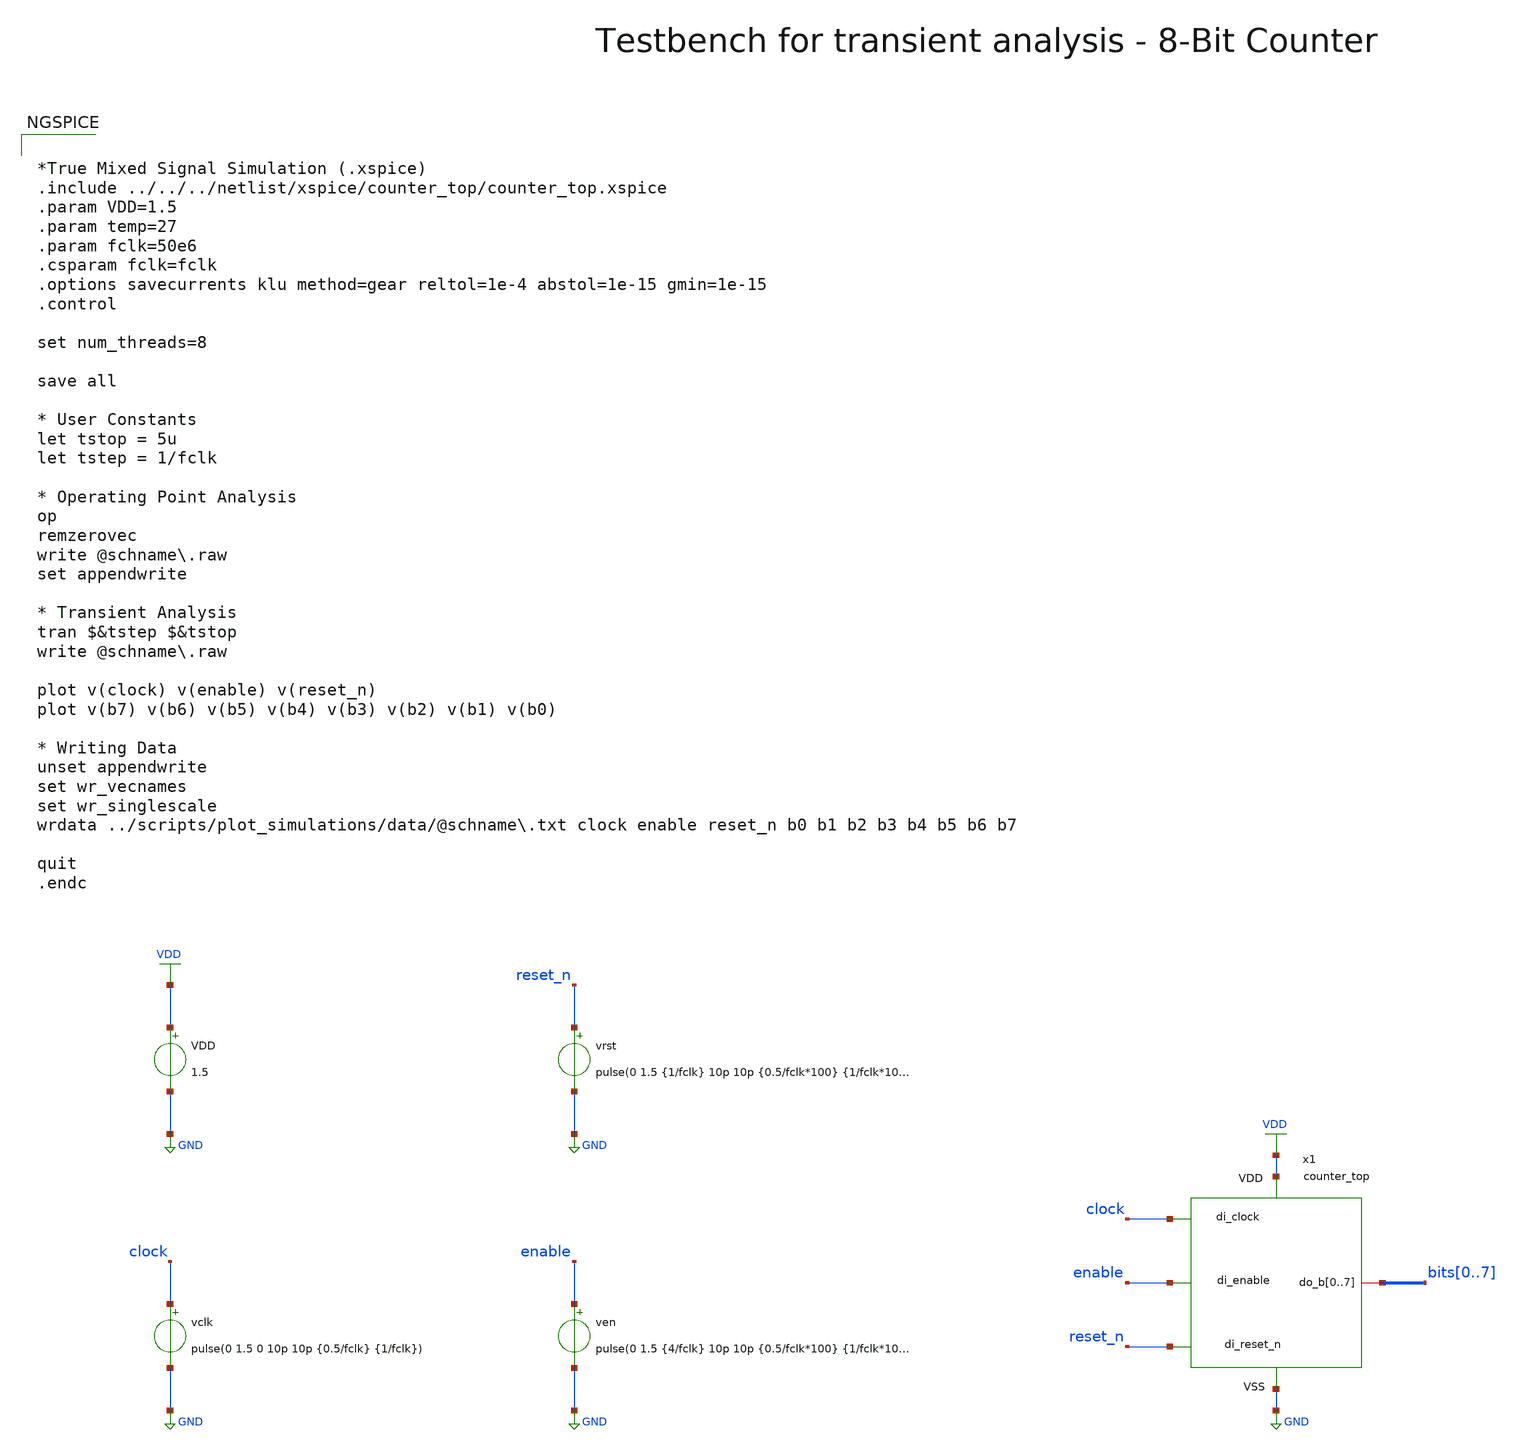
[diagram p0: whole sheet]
** sch_path: macros/counter/testbenches/xschem/counter_top_tb_tran.sch
**.subckt counter_top_tb_tran
VDD VDD GND 1.5
vclk clock GND pulse(0 1.5 0 10p 10p {0.5/fclk} {1/fclk})
vrst reset_n GND pulse(0 1.5 {1/fclk} 10p 10p {0.5/fclk*100} {1/fclk*100})
ven enable GND pulse(0 1.5 {4/fclk} 10p 10p {0.5/fclk*100} {1/fclk*100})
x1 VDD GND clock reset_n enable bits0 bits1 bits2 bits3 bits4 bits5 bits6 bits7 counter_top
**** begin user architecture code


*True Mixed Signal Simulation (.xspice)
.include ../../../netlist/xspice/counter_top/counter_top.xspice
.param VDD=1.5
.param temp=27
.param fclk=50e6
.csparam fclk=fclk
.options savecurrents klu method=gear reltol=1e-4 abstol=1e-15 gmin=1e-15
.control

set num_threads=8

save all

* User Constants
let tstop = 5u
let tstep = 1/fclk

* Operating Point Analysis
op
remzerovec
write @schname\.raw
set appendwrite

* Transient Analysis
tran $&tstep $&tstop
write @schname\.raw

plot v(clock) v(enable) v(reset_n)
plot v(b7) v(b6) v(b5) v(b4) v(b3) v(b2) v(b1) v(b0)

* Writing Data
unset appendwrite
set wr_vecnames
set wr_singlescale
wrdata ../scripts/plot_simulations/data/@schname\.txt clock enable reset_n b0 b1 b2 b3 b4 b5 b6 b7

quit
.endc


.lib cornerMOSlv.lib mos_tt
.lib cornerMOShv.lib mos_tt
.lib cornerHBT.lib hbt_typ
.lib cornerRES.lib res_typ
.lib cornerCAP.lib cap_typ
.lib cornerDIO.lib dio_tt

**** end user architecture code
**.ends
.GLOBAL GND
.GLOBAL VDD
.end
